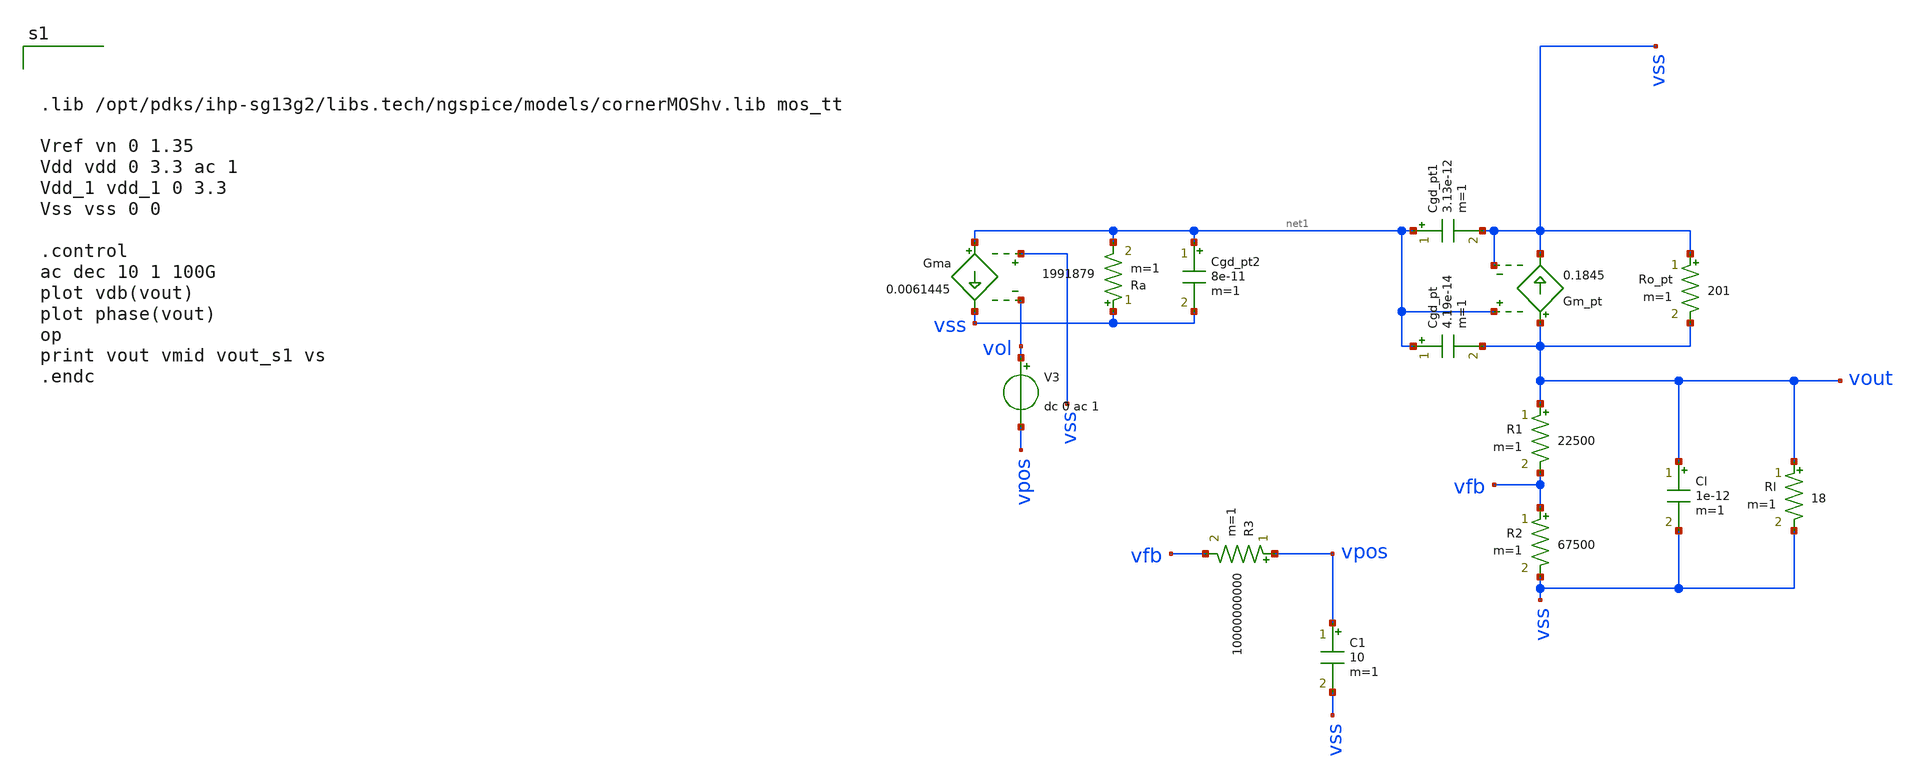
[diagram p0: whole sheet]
** sch_path: test/Tesis_notebooks/xschem/ldo_ol_tb_ss.sch
**.subckt ldo_ol_tb_ss
R3 vpos vfb 10000000000 m=1
C1 vpos vss 10 m=1
Ro_pt vss vout 201 m=1
Gm_pt vout vss net1 vss 0.1845
R1 vout vfb 22500 m=1
R2 vfb vss 67500 m=1
Gma net1 vss vss vol 0.0061445
Ra vss net1 1991879 m=1
Rl vout vss 18 m=1
Cgd_pt net1 vout 4.19e-14 m=1
Cl vout vss 1e-12 m=1
V3 vol vpos dc 0 ac 1
Cgd_pt1 net1 vss 3.13e-12 m=1
Cgd_pt2 net1 vss 8e-11 m=1
**** begin user architecture code



.lib /opt/pdks/ihp-sg13g2/libs.tech/ngspice/models/cornerMOShv.lib mos_tt

Vref vn 0 1.35
Vdd vdd 0 3.3 ac 1
Vdd_1 vdd_1 0 3.3
Vss vss 0 0

.control
ac dec 10 1 100G
plot vdb(vout)
plot phase(vout)
op
print vout vmid vout_s1 vs
.endc



**** end user architecture code
**.ends
.end
